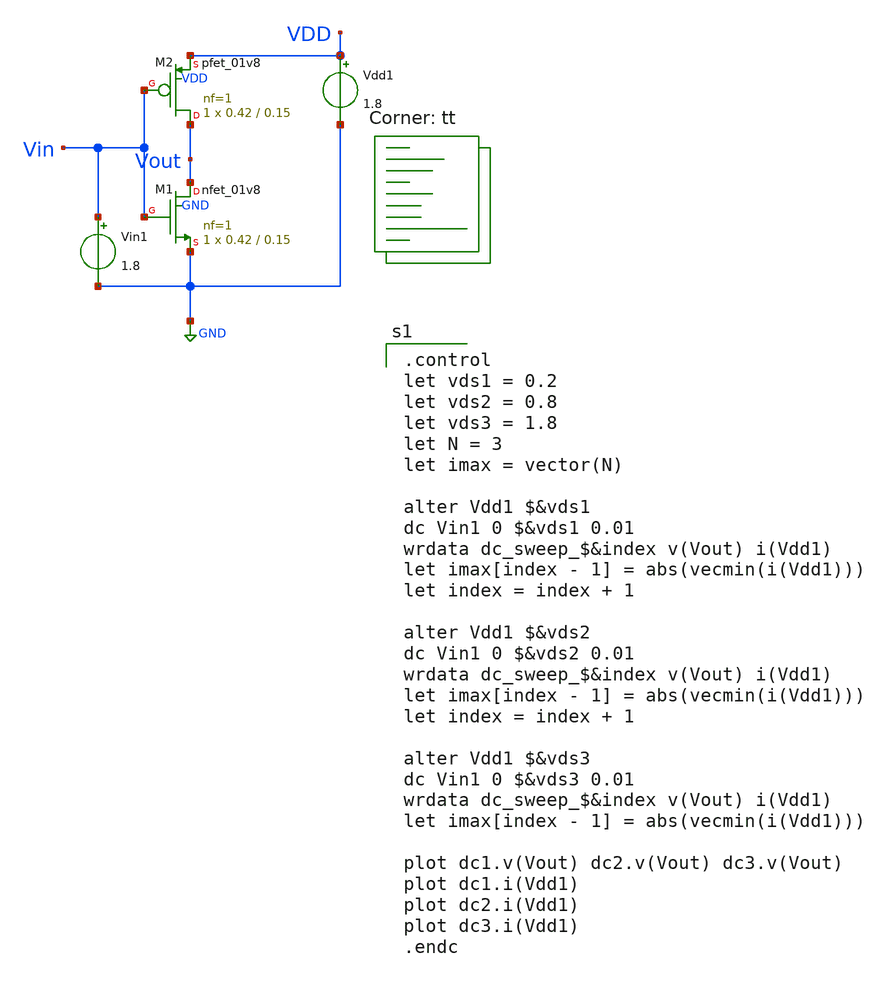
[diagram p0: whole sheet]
** sch_path: tut2/expt2_2/expt2_2.sch
**.subckt expt2_2
XM1 Vout Vin GND GND sky130_fd_pr__nfet_01v8 L=0.15 W=0.42 nf=1 ad='int((nf+1)/2) * W/nf * 0.29' as='int((nf+2)/2) * W/nf * 0.29'
+ pd='2*int((nf+1)/2) * (W/nf + 0.29)' ps='2*int((nf+2)/2) * (W/nf + 0.29)' nrd='0.29 / W' nrs='0.29 / W'
+ sa=0 sb=0 sd=0 mult=1 m=1
Vin1 Vin GND 1.8
XM2 Vout Vin VDD VDD sky130_fd_pr__pfet_01v8 L=0.15 W=0.42 nf=1 ad='int((nf+1)/2) * W/nf * 0.29' as='int((nf+2)/2) * W/nf * 0.29'
+ pd='2*int((nf+1)/2) * (W/nf + 0.29)' ps='2*int((nf+2)/2) * (W/nf + 0.29)' nrd='0.29 / W' nrs='0.29 / W'
+ sa=0 sb=0 sd=0 mult=1 m=1
Vdd1 VDD GND 1.8
**** begin user architecture code
.lib $::SKYWATER_MODELS/sky130.lib.spice tt

.control
let vds1 = 0.2
let vds2 = 0.8
let vds3 = 1.8
let N = 3
let imax = vector(N)

alter Vdd1 $&vds1
dc Vin1 0 $&vds1 0.01
wrdata dc_sweep_$&index v(Vout) i(Vdd1)
let imax[index - 1] = abs(vecmin(i(Vdd1)))
let index = index + 1

alter Vdd1 $&vds2
dc Vin1 0 $&vds2 0.01
wrdata dc_sweep_$&index v(Vout) i(Vdd1)
let imax[index - 1] = abs(vecmin(i(Vdd1)))
let index = index + 1

alter Vdd1 $&vds3
dc Vin1 0 $&vds3 0.01
wrdata dc_sweep_$&index v(Vout) i(Vdd1)
let imax[index - 1] = abs(vecmin(i(Vdd1)))

plot dc1.v(Vout) dc2.v(Vout) dc3.v(Vout)
plot dc1.i(Vdd1)
plot dc2.i(Vdd1)
plot dc3.i(Vdd1)
.endc

**** end user architecture code
**.ends
.GLOBAL GND
.end
